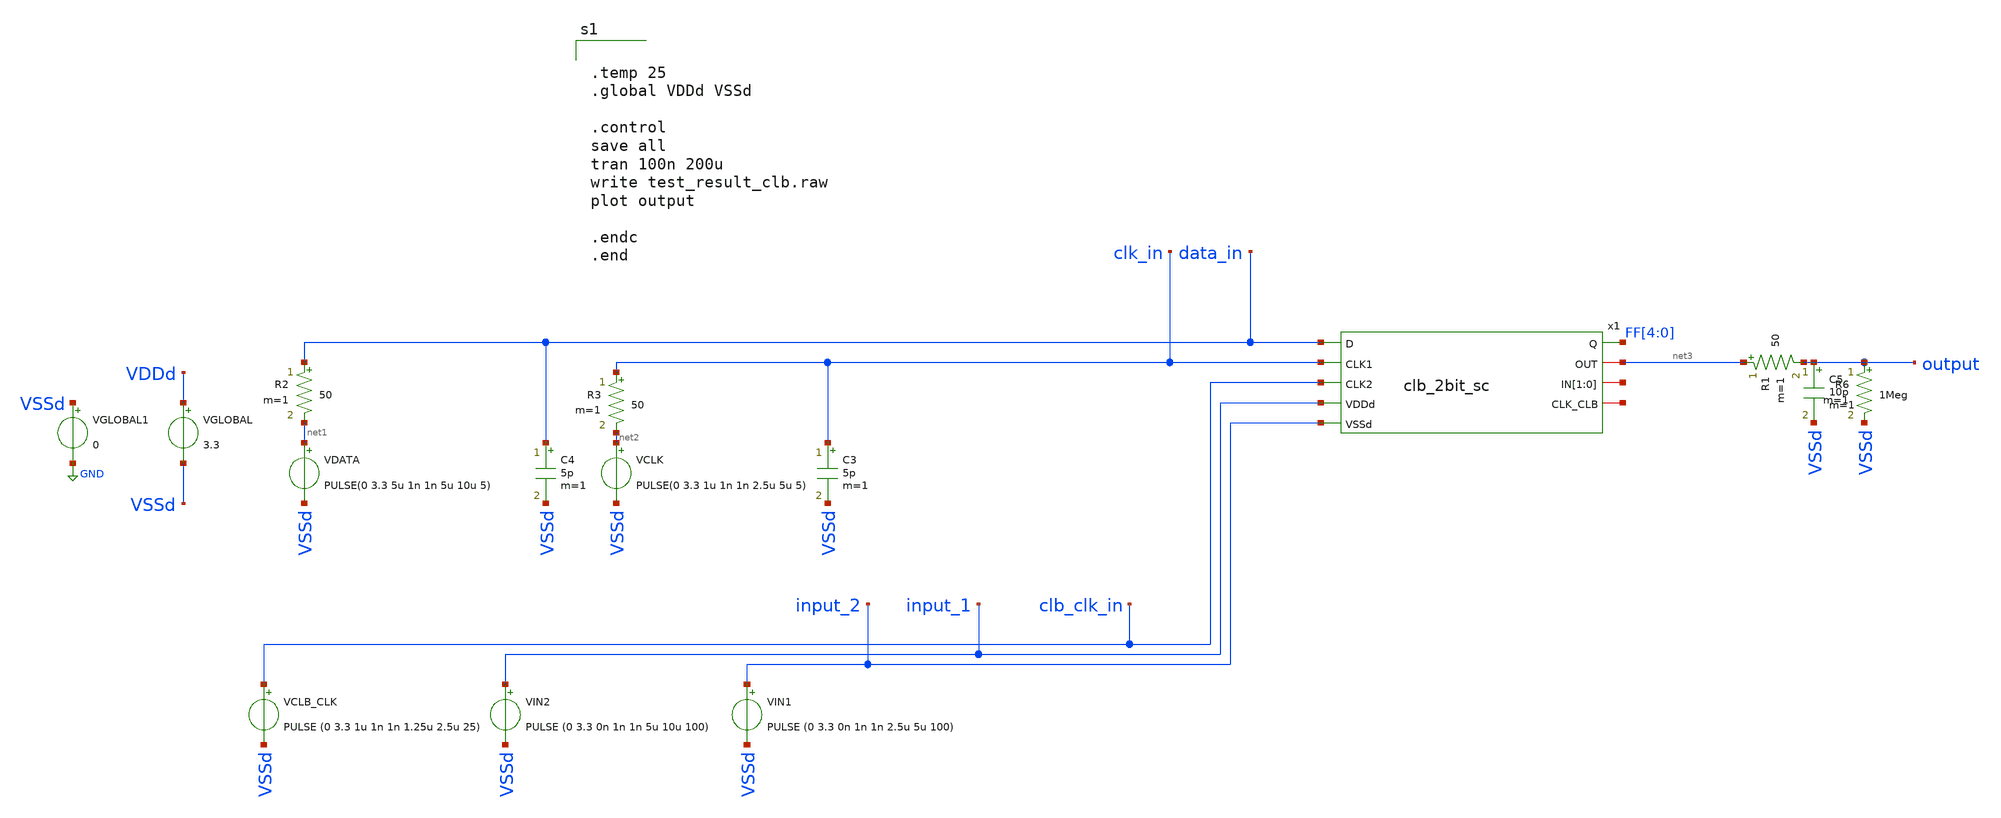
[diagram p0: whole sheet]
** sch_path: designs/libs/tb_fpga/tb_clb/clb_2bit_sc_tb.sch
**.subckt clb_2bit_sc_tb
C3 clk_in VSSd 5p m=1
C4 data_in VSSd 5p m=1
VCLK net2 VSSd PULSE(0 3.3 1u 1n 1n 2.5u 5u 5)
VDATA net1 VSSd PULSE(0 3.3 5u 1n 1n 5u 10u 5)
C5 output VSSd 10p m=1
R1 net3 output 50 m=1
R2 data_in net1 50 m=1
R3 clk_in net2 50 m=1
R6 output VSSd 1Meg m=1
VIN1 input_2 VSSd PULSE (0 3.3 0n 1n 1n 2.5u 5u 100)
VIN2 input_1 VSSd PULSE (0 3.3 0n 1n 1n 5u 10u 100)
VCLB_CLK clb_clk_in VSSd PULSE (0 3.3 1u 1n 1n 1.25u 2.5u 25)
x1 data_in clk_in clb_clk_in input_1 input_2 FF[4] net3 net4[1] net4[0] net5 clb_2bit_sc
VGLOBAL VDDd VSSd 3.3
VGLOBAL1 VSSd GND 0
**** begin user architecture code


.temp 25
.global VDDd VSSd

.control
save all
tran 100n 200u
write test_result_clb.raw
plot output

.endc
.end



.include $::180MCU_MODELS/design.ngspice
.include /foss/pdks/gf180mcuD/libs.ref/gf180mcu_fd_sc_mcu9t5v0/spice/gf180mcu_fd_sc_mcu9t5v0.spice
.lib $::180MCU_MODELS/sm141064.ngspice typical
.lib $::180MCU_MODELS/sm141064.ngspice cap_mim
.lib $::180MCU_MODELS/sm141064.ngspice res_typical
.lib $::180MCU_MODELS/sm141064.ngspice moscap_typical
.lib $::180MCU_MODELS/sm141064.ngspice mimcap_typical
* .lib $::180MCU_MODELS/sm141064.ngspice res_statistical

**** end user architecture code
**.ends
.GLOBAL GND
.end
